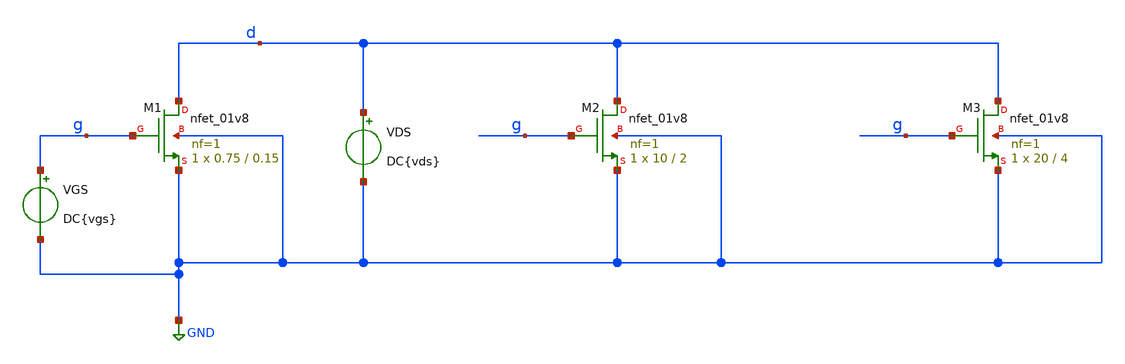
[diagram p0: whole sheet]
** sch_path: Tp1/Mis Simulaciones/tp1_1.sch
**.subckt tp1_1
XM1 d g GND GND sky130_fd_pr__nfet_01v8 L=0.15 W=0.75 nf=1 ad='int((nf+1)/2) * W/nf * 0.29' as='int((nf+2)/2) * W/nf * 0.29'
+ pd='2*int((nf+1)/2) * (W/nf + 0.29)' ps='2*int((nf+2)/2) * (W/nf + 0.29)' nrd='0.29 / W' nrs='0.29 / W'
+ sa=0 sb=0 sd=0 mult=1 m=1
VGS g GND DC{vgs}
VDS d GND DC{vds}
XM2 d g GND GND sky130_fd_pr__nfet_01v8 L=2 W=10 nf=1 ad='int((nf+1)/2) * W/nf * 0.29' as='int((nf+2)/2) * W/nf * 0.29'
+ pd='2*int((nf+1)/2) * (W/nf + 0.29)' ps='2*int((nf+2)/2) * (W/nf + 0.29)' nrd='0.29 / W' nrs='0.29 / W'
+ sa=0 sb=0 sd=0 mult=1 m=1
XM3 d g GND GND sky130_fd_pr__nfet_01v8 L=4 W=20 nf=1 ad='int((nf+1)/2) * W/nf * 0.29' as='int((nf+2)/2) * W/nf * 0.29'
+ pd='2*int((nf+1)/2) * (W/nf + 0.29)' ps='2*int((nf+2)/2) * (W/nf + 0.29)' nrd='0.29 / W' nrs='0.29 / W'
+ sa=0 sb=0 sd=0 mult=1 m=1
**** begin user architecture code



* Parameters
.param vds = 1.8
.param vgs = 0.9
.options TEMPS = 27.0

* Models
.lib ~/skywater/skywater-pdk/libraries/sky130_fd_pr_ngspice/latest/models/corners/sky130.lib TT

* Data to save
.save all  @M.XM1.msky130_fd_pr__nfet_01v8[id]  @M.XM1.msky130_fd_pr__nfet_01v8[gm]  @M.XM1.msky130_fd_pr__nfet_01v8[vth]  @M.XM1.msky130_fd_pr__nfet_01v8[vds]  @M.XM1.msky130_fd_pr__nfet_01v8[vdsat]  @M.XM1.msky130_fd_pr__nfet_01v8[vgs]  @M.XM1.msky130_fd_pr__nfet_01v8[cgg]  @M.XM2.msky130_fd_pr__nfet_01v8[id]  @M.XM2.msky130_fd_pr__nfet_01v8[gm]  @M.XM2.msky130_fd_pr__nfet_01v8[vth]  @M.XM2.msky130_fd_pr__nfet_01v8[vds]  @M.XM2.msky130_fd_pr__nfet_01v8[vdsat]  @M.XM2.msky130_fd_pr__nfet_01v8[vgs]  @M.XM2.msky130_fd_pr__nfet_01v8[cgg]  @M.XM3.msky130_fd_pr__nfet_01v8[id]  @M.XM3.msky130_fd_pr__nfet_01v8[gm]  @M.XM3.msky130_fd_pr__nfet_01v8[vth]  @M.XM3.msky130_fd_pr__nfet_01v8[vds]  @M.XM3.msky130_fd_pr__nfet_01v8[vdsat]  @M.XM3.msky130_fd_pr__nfet_01v8[vgs]  @M.XM3.msky130_fd_pr__nfet_01v8[cgg]

* Simulation
.control
  dc VDS 0 1.8 0.01 VGS 0 1.8 0.3
  setplot dc1
  plot @M.XM1.msky130_fd_pr__nfet_01v8[id] @M.XM2.msky130_fd_pr__nfet_01v8[id] @M.XM3.msky130_fd_pr__nfet_01v8[id]
+ ylabel Id xlabel Vds title 'Id vs Vds vs Vgs'
  set filetype = ascii
  write tp1_1_dc1.raw

  reset
  dc VGS 0 1.8 0.01
  setplot dc2
  plot @M.XM1.msky130_fd_pr__nfet_01v8[id] @M.XM2.msky130_fd_pr__nfet_01v8[id] @M.XM3.msky130_fd_pr__nfet_01v8[id]
+ ylabel Id xlabel Vgs title 'Id vs Vgs (escala lineal)'
  plot @M.XM1.msky130_fd_pr__nfet_01v8[id] @M.XM2.msky130_fd_pr__nfet_01v8[id] @M.XM3.msky130_fd_pr__nfet_01v8[id]
+ ylog ylabel log(Id) xlabel Vgs title 'Id (escala log.) vs Vgs'
  plot @M.XM1.msky130_fd_pr__nfet_01v8[gm]/@M.XM1.msky130_fd_pr__nfet_01v8[id] vs @M.XM1.msky130_fd_pr__nfet_01v8[id]
+ @M.XM2.msky130_fd_pr__nfet_01v8[gm]/@M.XM2.msky130_fd_pr__nfet_01v8[id] vs @M.XM2.msky130_fd_pr__nfet_01v8[id]
+ @M.XM3.msky130_fd_pr__nfet_01v8[gm]/@M.XM3.msky130_fd_pr__nfet_01v8[id] vs @M.XM3.msky130_fd_pr__nfet_01v8[id]
+ xlog ylabel gm/Id xlabel Id title 'gm/Id vs Id (escala log)'
  plot @M.XM1.msky130_fd_pr__nfet_01v8[gm]/@M.XM1.msky130_fd_pr__nfet_01v8[id] vs @M.XM1.msky130_fd_pr__nfet_01v8[vgs]
+ @M.XM2.msky130_fd_pr__nfet_01v8[gm]/@M.XM2.msky130_fd_pr__nfet_01v8[id] vs @M.XM2.msky130_fd_pr__nfet_01v8[vgs]
+ @M.XM3.msky130_fd_pr__nfet_01v8[gm]/@M.XM3.msky130_fd_pr__nfet_01v8[id] vs @M.XM3.msky130_fd_pr__nfet_01v8[vgs]
+ ylabel gm/Id xlabel Vgs title 'gm/Id vs Vgs'
  plot @M.XM1.msky130_fd_pr__nfet_01v8[gm]/@M.Xm1.msky130_fd_pr__nfet_01v8[id] vs @M.XM1.msky130_fd_pr__nfet_01v8[id]
+ @M.XM2.msky130_fd_pr__nfet_01v8[gm]/@M.Xm2.msky130_fd_pr__nfet_01v8[id] vs @M.XM2.msky130_fd_pr__nfet_01v8[id]
+ @M.XM3.msky130_fd_pr__nfet_01v8[gm]/@M.Xm3.msky130_fd_pr__nfet_01v8[id] vs @M.XM3.msky130_fd_pr__nfet_01v8[id]
+ ylabel gm/Id xlabel Id title 'gm/Id vs Id'
  set filetype = ascii
  write tp1_1_dc2.raw

  alterparam vds = 0
  reset
  dc VGS -1.8 1.8 0.01
  setplot dc3
  plot @M.XM1.msky130_fd_pr__nfet_01v8[cgg] @M.XM2.msky130_fd_pr__nfet_01v8[cgg]
+ @M.XM3.msky130_fd_pr__nfet_01v8[cgg] ylabel Cgg xlabel Vgs
  set filetype = ascii
  write tp1_1_dc3.raw

  reset
  unset filetype
  op
  save all
  write tp1_1.raw

.endc

.end


**** end user architecture code
**.ends
.GLOBAL GND
.end
